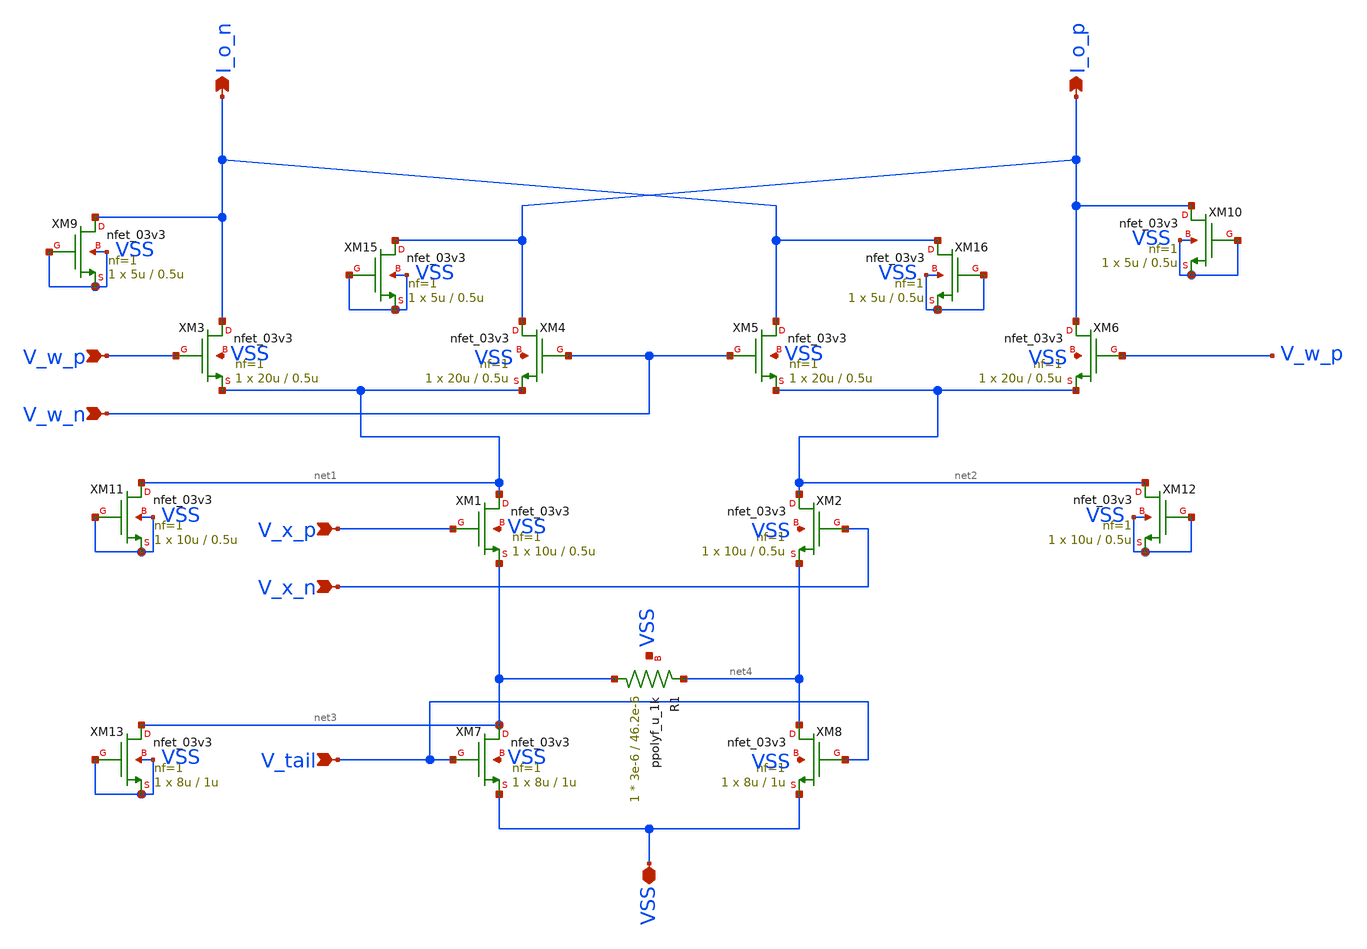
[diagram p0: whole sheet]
** sch_path: lvs/schematics/gilbert_multiplier_current.sch
**.subckt gilbert_multiplier_current V_x_p V_x_n V_tail VSS V_w_p V_w_n I_o_n I_o_p
*.ipin V_x_p
*.ipin V_x_n
*.ipin V_tail
*.iopin VSS
*.ipin V_w_p
*.ipin V_w_n
*.opin I_o_n
*.opin I_o_p
XM1 net1 V_x_p net3 VSS nfet_03v3 L=0.5u W=10u nf=1 ad='int((nf+1)/2) * W/nf * 0.18u' as='int((nf+2)/2) * W/nf * 0.18u'
+ pd='2*int((nf+1)/2) * (W/nf + 0.18u)' ps='2*int((nf+2)/2) * (W/nf + 0.18u)' nrd='0.18u / W' nrs='0.18u / W'
+ sa=0 sb=0 sd=0 m=1
XM2 net2 V_x_n net4 VSS nfet_03v3 L=0.5u W=10u nf=1 ad='int((nf+1)/2) * W/nf * 0.18u' as='int((nf+2)/2) * W/nf * 0.18u'
+ pd='2*int((nf+1)/2) * (W/nf + 0.18u)' ps='2*int((nf+2)/2) * (W/nf + 0.18u)' nrd='0.18u / W' nrs='0.18u / W'
+ sa=0 sb=0 sd=0 m=1
XM3 I_o_n V_w_p net1 VSS nfet_03v3 L=0.5u W=20u nf=1 ad='int((nf+1)/2) * W/nf * 0.18u' as='int((nf+2)/2) * W/nf * 0.18u'
+ pd='2*int((nf+1)/2) * (W/nf + 0.18u)' ps='2*int((nf+2)/2) * (W/nf + 0.18u)' nrd='0.18u / W' nrs='0.18u / W'
+ sa=0 sb=0 sd=0 m=1
XM4 I_o_p V_w_n net1 VSS nfet_03v3 L=0.5u W=20u nf=1 ad='int((nf+1)/2) * W/nf * 0.18u' as='int((nf+2)/2) * W/nf * 0.18u'
+ pd='2*int((nf+1)/2) * (W/nf + 0.18u)' ps='2*int((nf+2)/2) * (W/nf + 0.18u)' nrd='0.18u / W' nrs='0.18u / W'
+ sa=0 sb=0 sd=0 m=1
XM5 I_o_n V_w_n net2 VSS nfet_03v3 L=0.5u W=20u nf=1 ad='int((nf+1)/2) * W/nf * 0.18u' as='int((nf+2)/2) * W/nf * 0.18u'
+ pd='2*int((nf+1)/2) * (W/nf + 0.18u)' ps='2*int((nf+2)/2) * (W/nf + 0.18u)' nrd='0.18u / W' nrs='0.18u / W'
+ sa=0 sb=0 sd=0 m=1
XM6 I_o_p V_w_p net2 VSS nfet_03v3 L=0.5u W=20u nf=1 ad='int((nf+1)/2) * W/nf * 0.18u' as='int((nf+2)/2) * W/nf * 0.18u'
+ pd='2*int((nf+1)/2) * (W/nf + 0.18u)' ps='2*int((nf+2)/2) * (W/nf + 0.18u)' nrd='0.18u / W' nrs='0.18u / W'
+ sa=0 sb=0 sd=0 m=1
XM7 net3 V_tail VSS VSS nfet_03v3 L=1u W=8u nf=1 ad='int((nf+1)/2) * W/nf * 0.18u' as='int((nf+2)/2) * W/nf * 0.18u'
+ pd='2*int((nf+1)/2) * (W/nf + 0.18u)' ps='2*int((nf+2)/2) * (W/nf + 0.18u)' nrd='0.18u / W' nrs='0.18u / W'
+ sa=0 sb=0 sd=0 m=1
XM8 net4 V_tail VSS VSS nfet_03v3 L=1u W=8u nf=1 ad='int((nf+1)/2) * W/nf * 0.18u' as='int((nf+2)/2) * W/nf * 0.18u'
+ pd='2*int((nf+1)/2) * (W/nf + 0.18u)' ps='2*int((nf+2)/2) * (W/nf + 0.18u)' nrd='0.18u / W' nrs='0.18u / W'
+ sa=0 sb=0 sd=0 m=1
XR1 net3 net4 VSS ppolyf_u_1k r_width=3e-6 r_length=46.2e-6 m=1
XM9 I_o_n VSS VSS VSS nfet_03v3 L=0.5u W=5u nf=1 ad='int((nf+1)/2) * W/nf * 0.18u' as='int((nf+2)/2) * W/nf * 0.18u'
+ pd='2*int((nf+1)/2) * (W/nf + 0.18u)' ps='2*int((nf+2)/2) * (W/nf + 0.18u)' nrd='0.18u / W' nrs='0.18u / W'
+ sa=0 sb=0 sd=0 m=1
XM10 I_o_p VSS VSS VSS nfet_03v3 L=0.5u W=5u nf=1 ad='int((nf+1)/2) * W/nf * 0.18u' as='int((nf+2)/2) * W/nf * 0.18u'
+ pd='2*int((nf+1)/2) * (W/nf + 0.18u)' ps='2*int((nf+2)/2) * (W/nf + 0.18u)' nrd='0.18u / W' nrs='0.18u / W'
+ sa=0 sb=0 sd=0 m=1
XM11 net1 VSS VSS VSS nfet_03v3 L=0.5u W=10u nf=1 ad='int((nf+1)/2) * W/nf * 0.18u' as='int((nf+2)/2) * W/nf * 0.18u'
+ pd='2*int((nf+1)/2) * (W/nf + 0.18u)' ps='2*int((nf+2)/2) * (W/nf + 0.18u)' nrd='0.18u / W' nrs='0.18u / W'
+ sa=0 sb=0 sd=0 m=1
XM12 net2 VSS VSS VSS nfet_03v3 L=0.5u W=10u nf=1 ad='int((nf+1)/2) * W/nf * 0.18u' as='int((nf+2)/2) * W/nf * 0.18u'
+ pd='2*int((nf+1)/2) * (W/nf + 0.18u)' ps='2*int((nf+2)/2) * (W/nf + 0.18u)' nrd='0.18u / W' nrs='0.18u / W'
+ sa=0 sb=0 sd=0 m=1
XM13 net3 VSS VSS VSS nfet_03v3 L=1u W=8u nf=1 ad='int((nf+1)/2) * W/nf * 0.18u' as='int((nf+2)/2) * W/nf * 0.18u'
+ pd='2*int((nf+1)/2) * (W/nf + 0.18u)' ps='2*int((nf+2)/2) * (W/nf + 0.18u)' nrd='0.18u / W' nrs='0.18u / W'
+ sa=0 sb=0 sd=0 m=1
XM15 I_o_p VSS VSS VSS nfet_03v3 L=0.5u W=5u nf=1 ad='int((nf+1)/2) * W/nf * 0.18u' as='int((nf+2)/2) * W/nf * 0.18u'
+ pd='2*int((nf+1)/2) * (W/nf + 0.18u)' ps='2*int((nf+2)/2) * (W/nf + 0.18u)' nrd='0.18u / W' nrs='0.18u / W'
+ sa=0 sb=0 sd=0 m=1
XM16 I_o_n VSS VSS VSS nfet_03v3 L=0.5u W=5u nf=1 ad='int((nf+1)/2) * W/nf * 0.18u' as='int((nf+2)/2) * W/nf * 0.18u'
+ pd='2*int((nf+1)/2) * (W/nf + 0.18u)' ps='2*int((nf+2)/2) * (W/nf + 0.18u)' nrd='0.18u / W' nrs='0.18u / W'
+ sa=0 sb=0 sd=0 m=1
**.ends
.end
